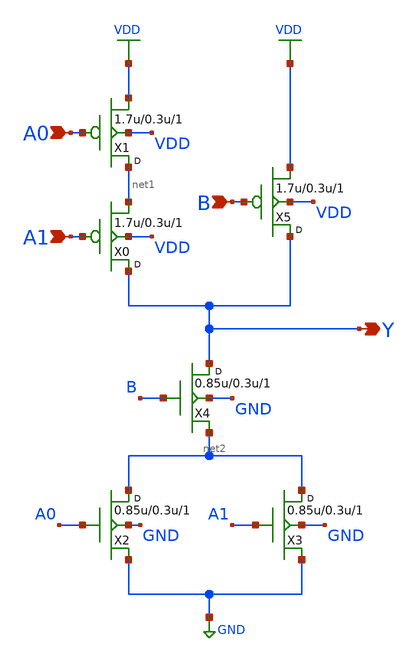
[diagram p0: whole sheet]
** sch_path: gf180mcu_osu_sc_gp12t3v3/cells/oai21/gf180mcu_osu_sc_gp12t3v3__oai21_1.sch
**.subckt gf180mcu_osu_sc_gp12t3v3__oai21_1 A0 A1 Y B
*.ipin A0
*.ipin A1
*.opin Y
*.ipin B
X1 net1 A0 VDD VDD pfet_03p3 w=1.7u l=0.3u m=1
X0 Y A1 net1 VDD pfet_03p3 w=1.7u l=0.3u m=1
X2 net2 A0 GND GND nfet_03p3 w=0.85u l=0.3u m=1
X3 net2 A1 GND GND nfet_03p3 w=0.85u l=0.3u m=1
X4 Y B net2 GND nfet_03p3 w=0.85u l=0.3u m=1
X5 Y B VDD VDD pfet_03p3 w=1.7u l=0.3u m=1
**.ends
.GLOBAL VDD
.GLOBAL GND
.end
